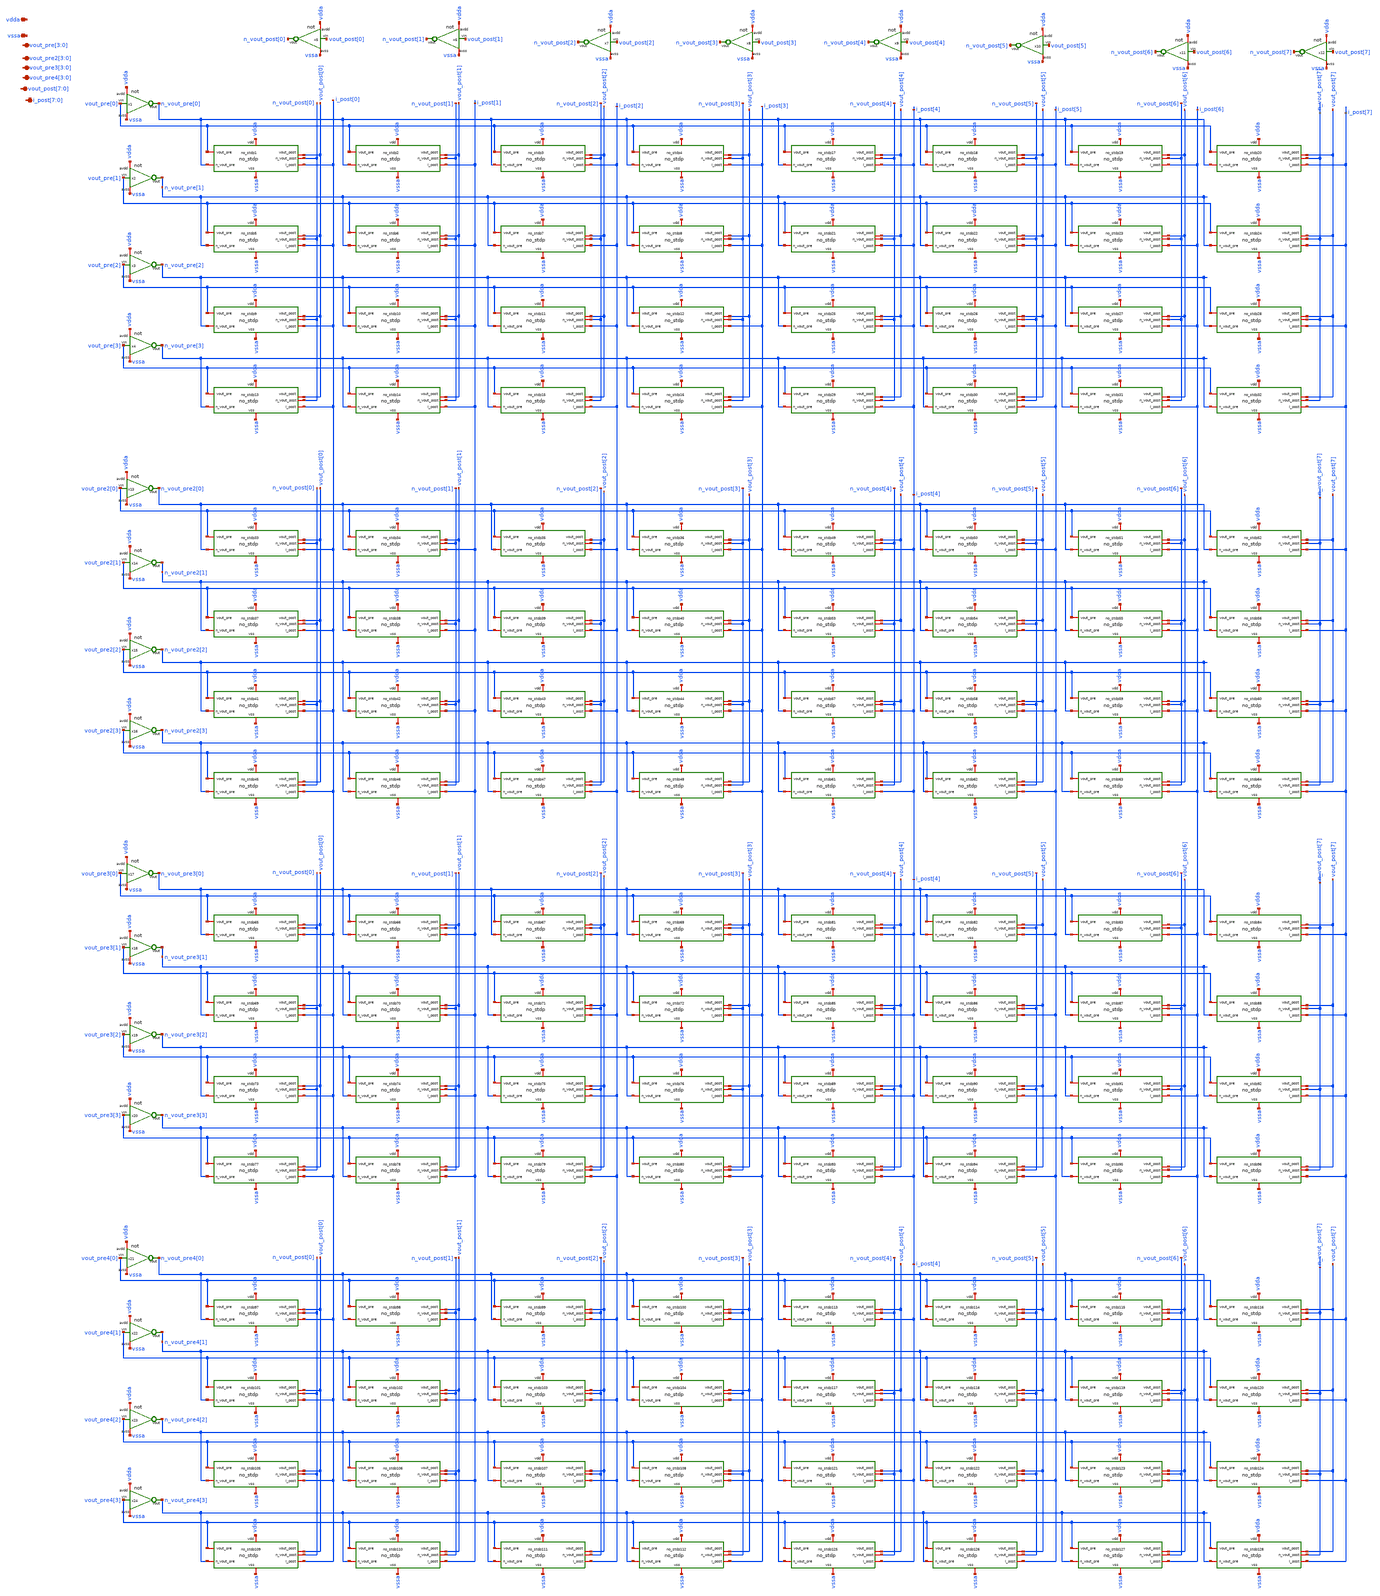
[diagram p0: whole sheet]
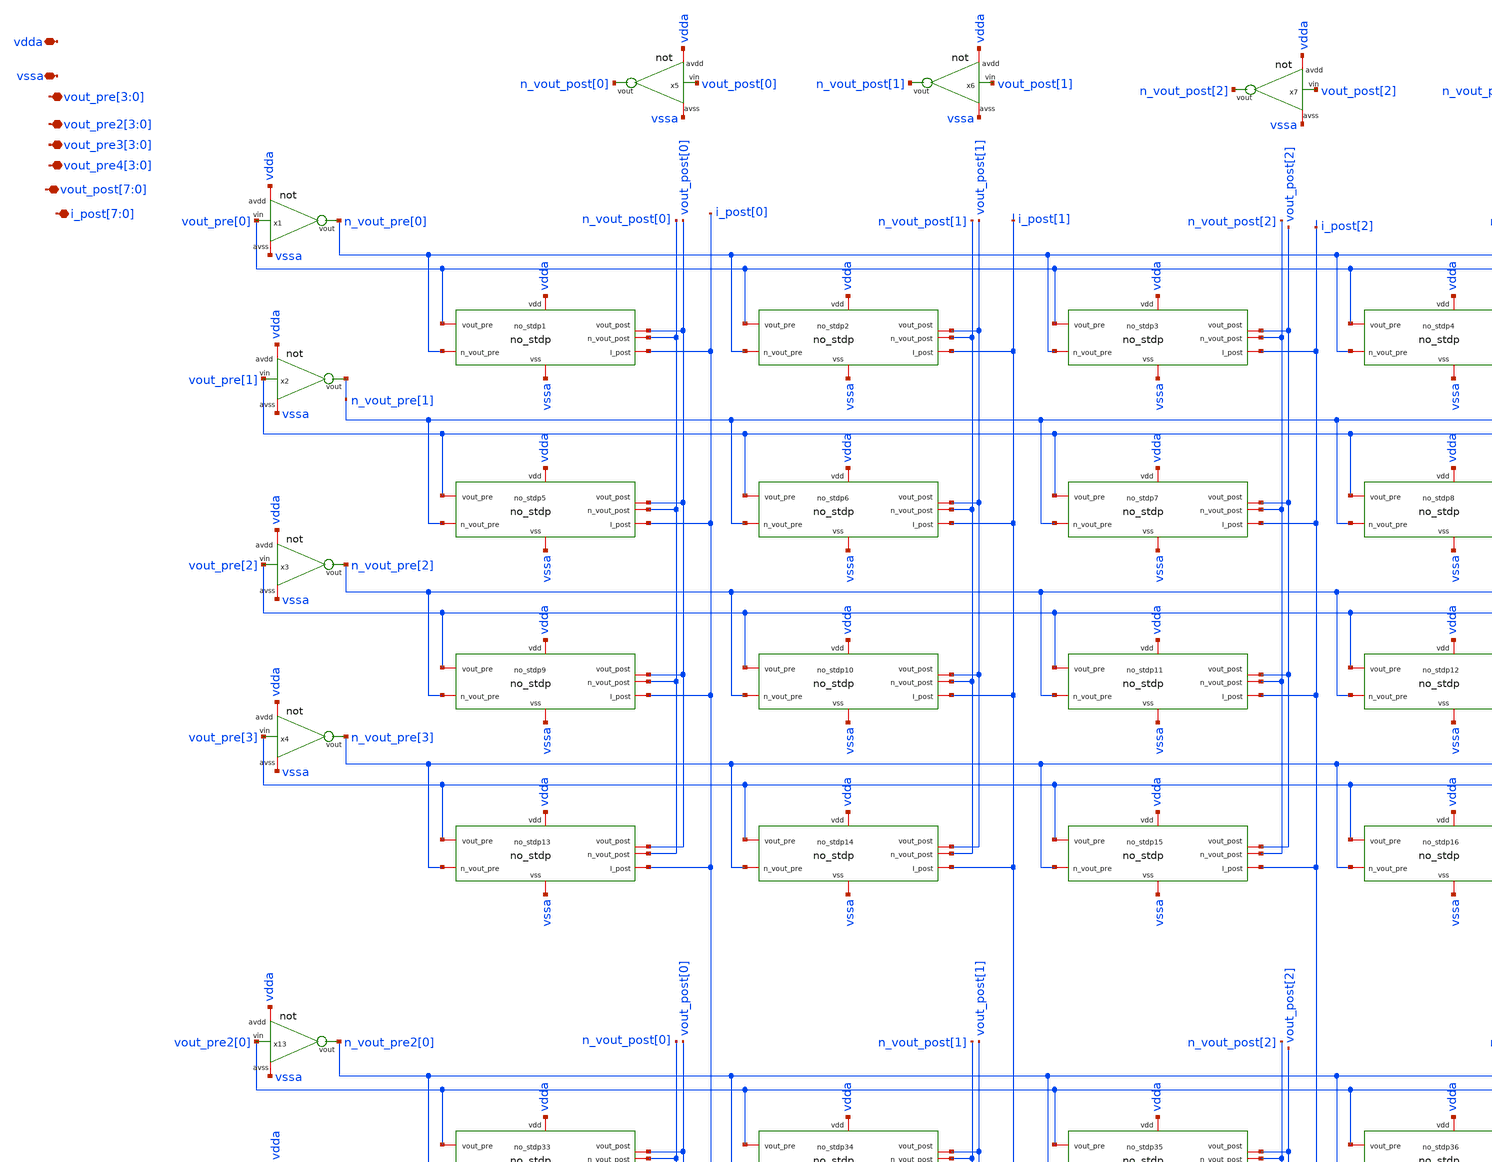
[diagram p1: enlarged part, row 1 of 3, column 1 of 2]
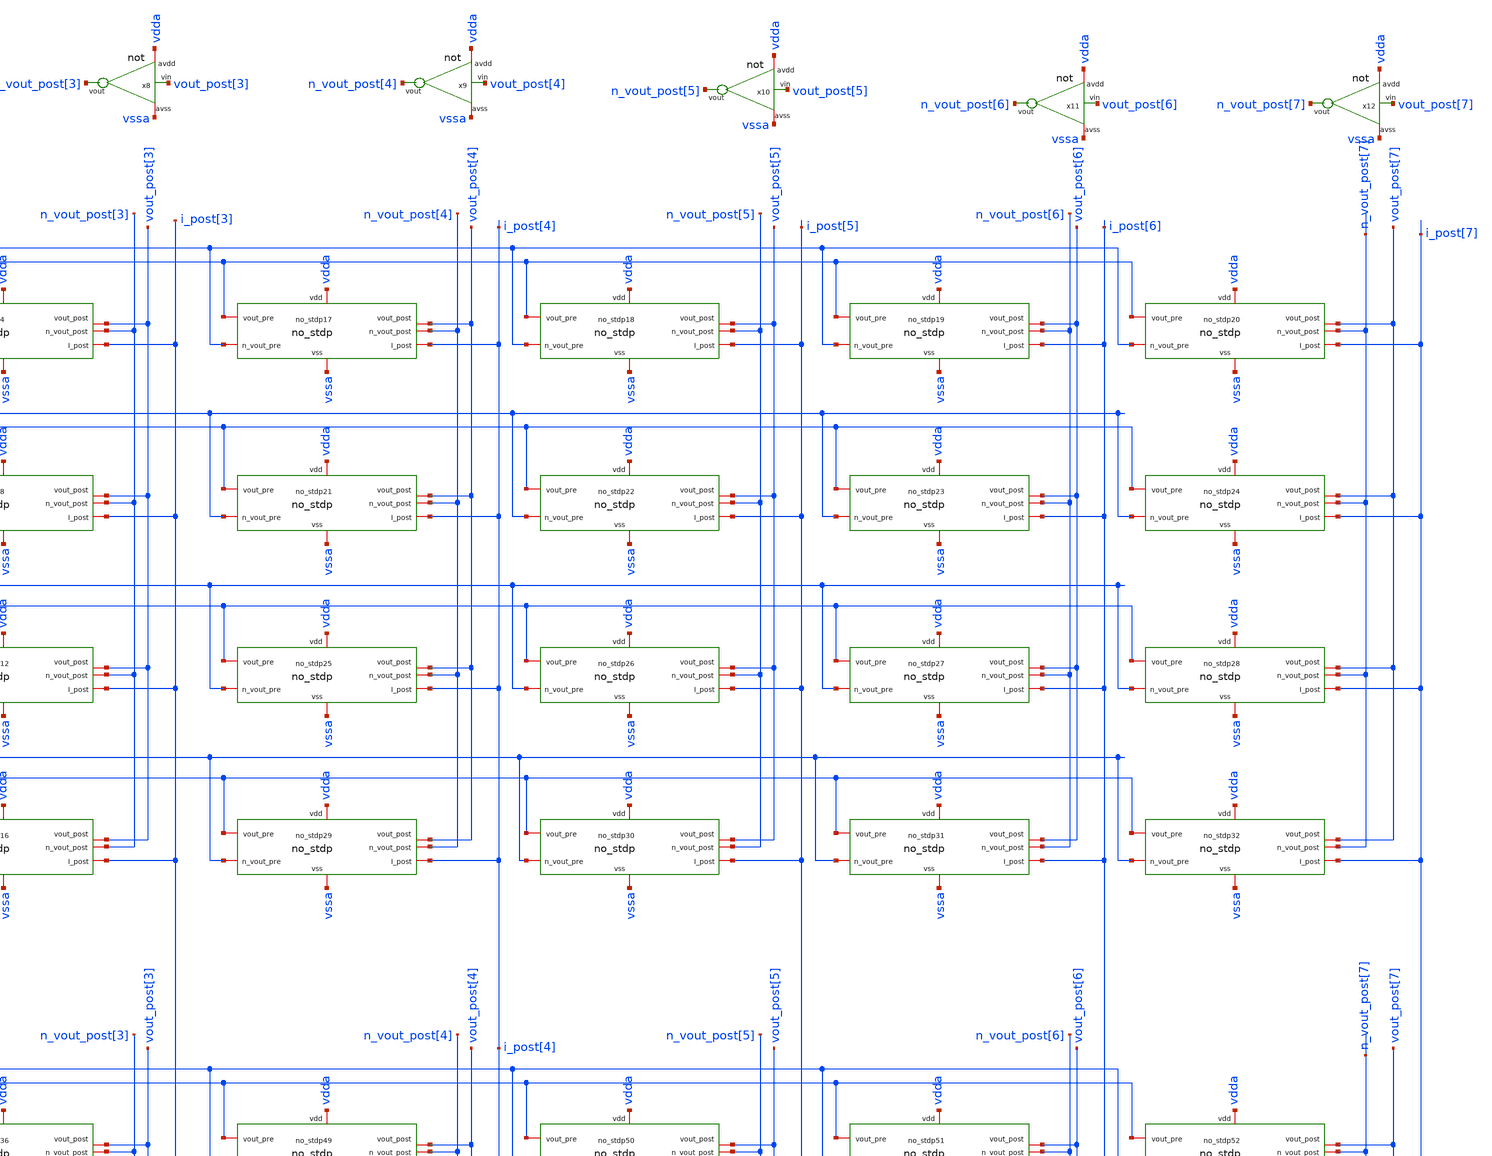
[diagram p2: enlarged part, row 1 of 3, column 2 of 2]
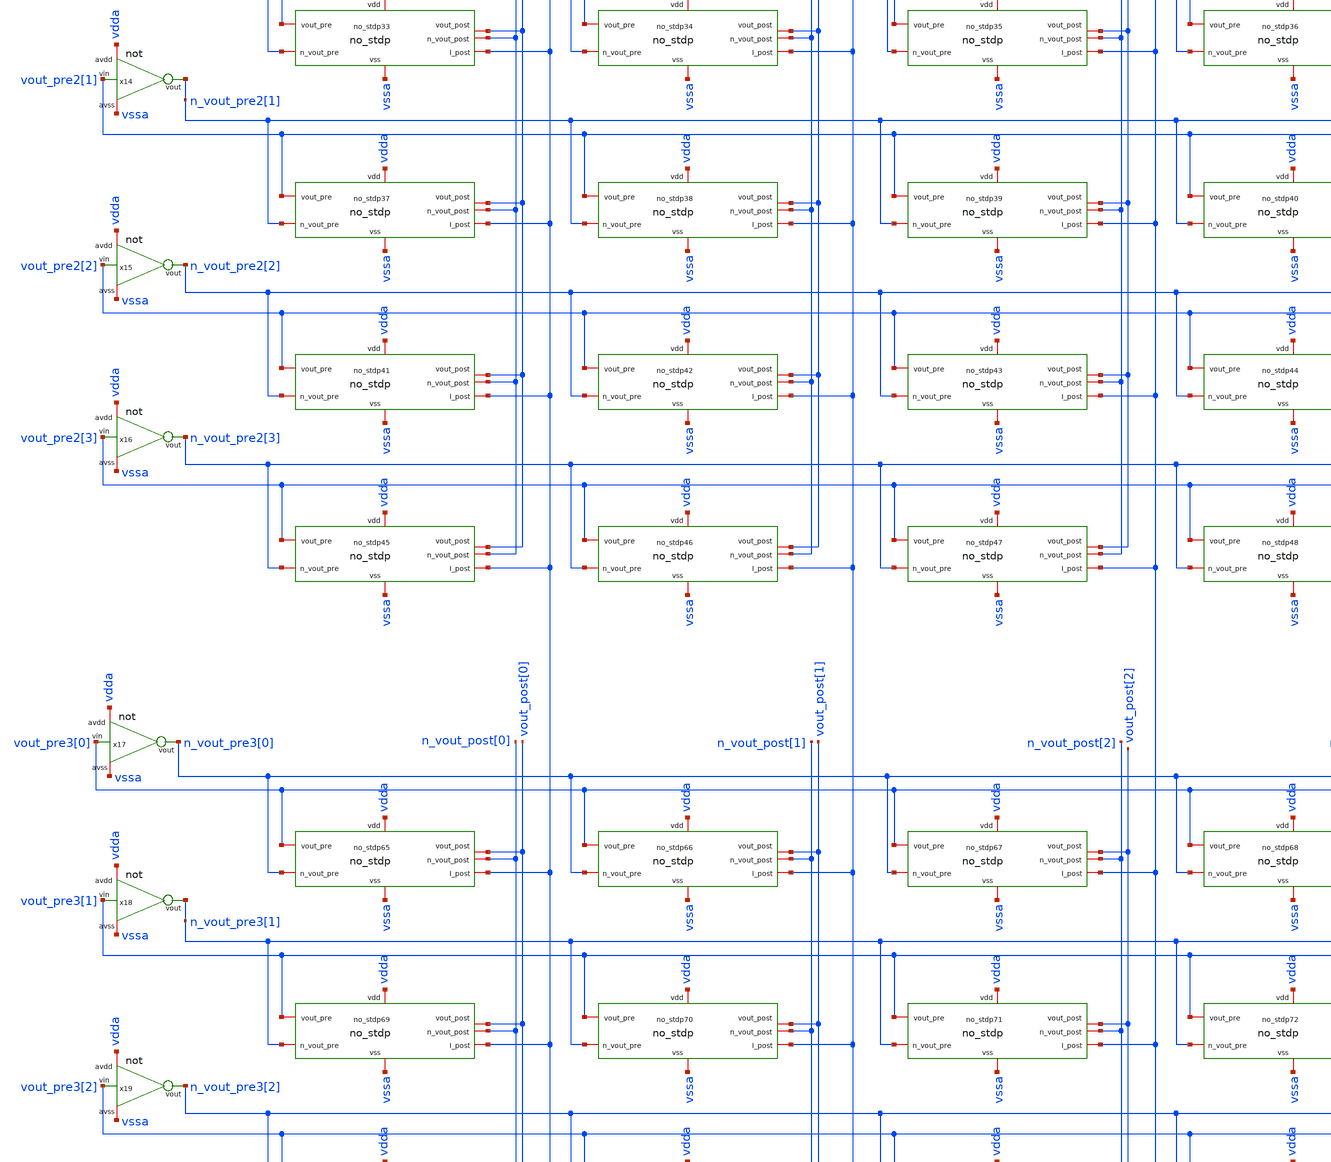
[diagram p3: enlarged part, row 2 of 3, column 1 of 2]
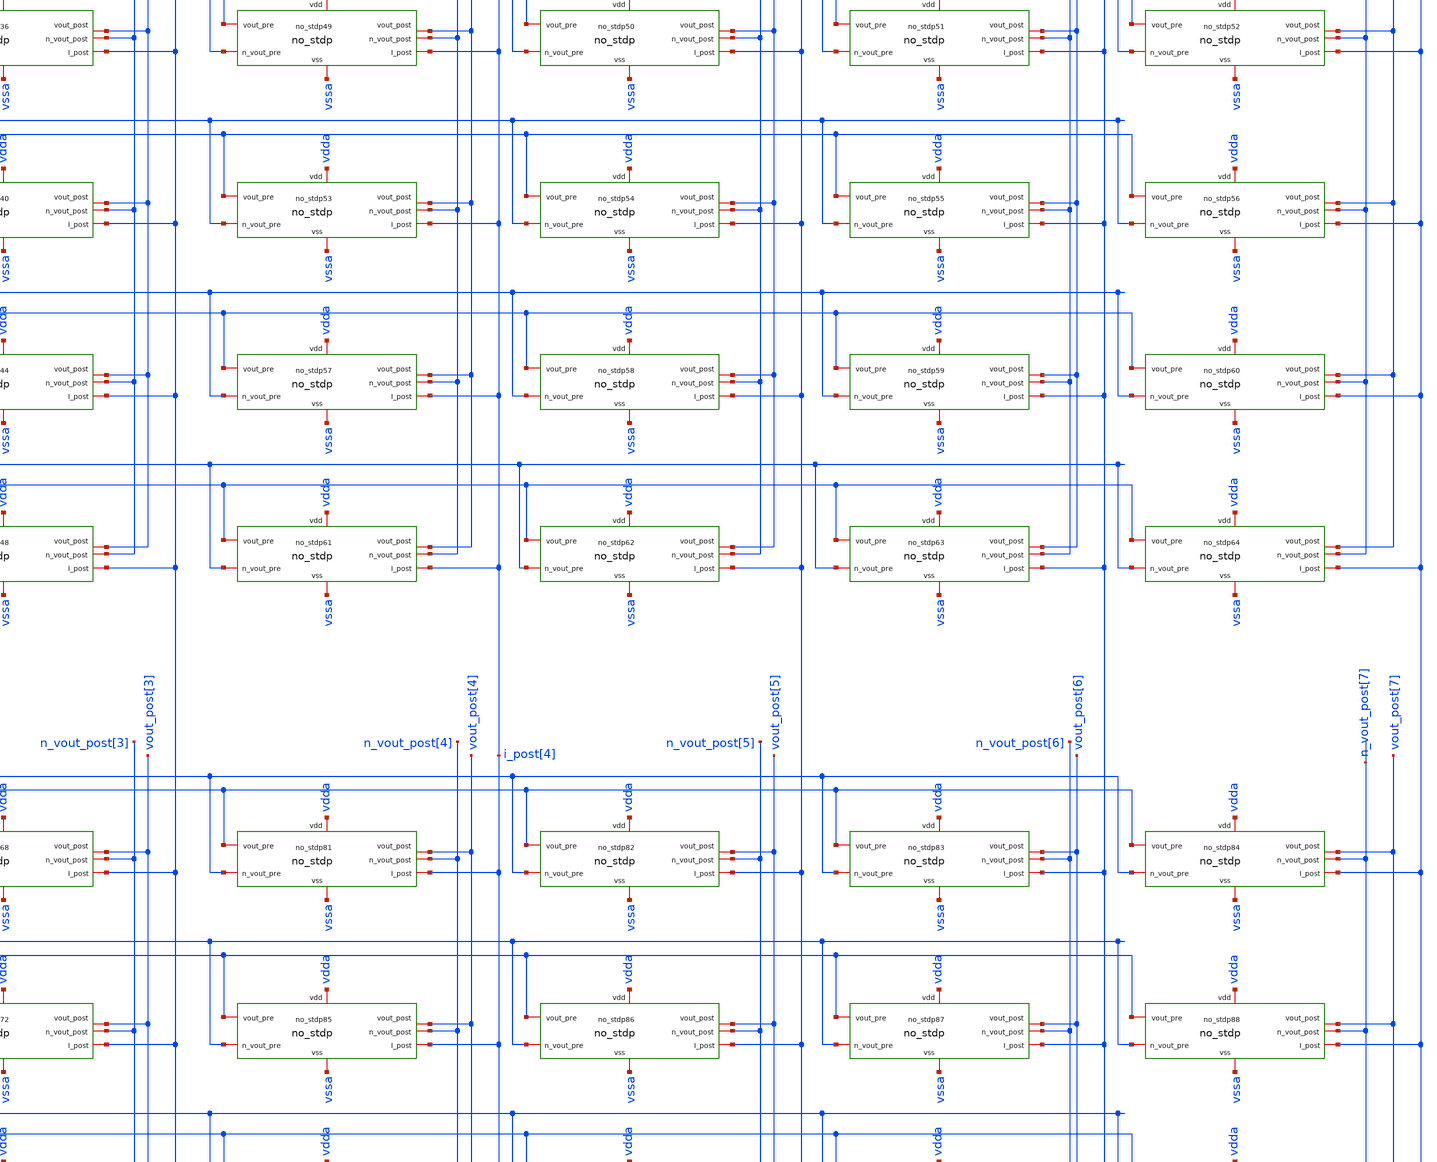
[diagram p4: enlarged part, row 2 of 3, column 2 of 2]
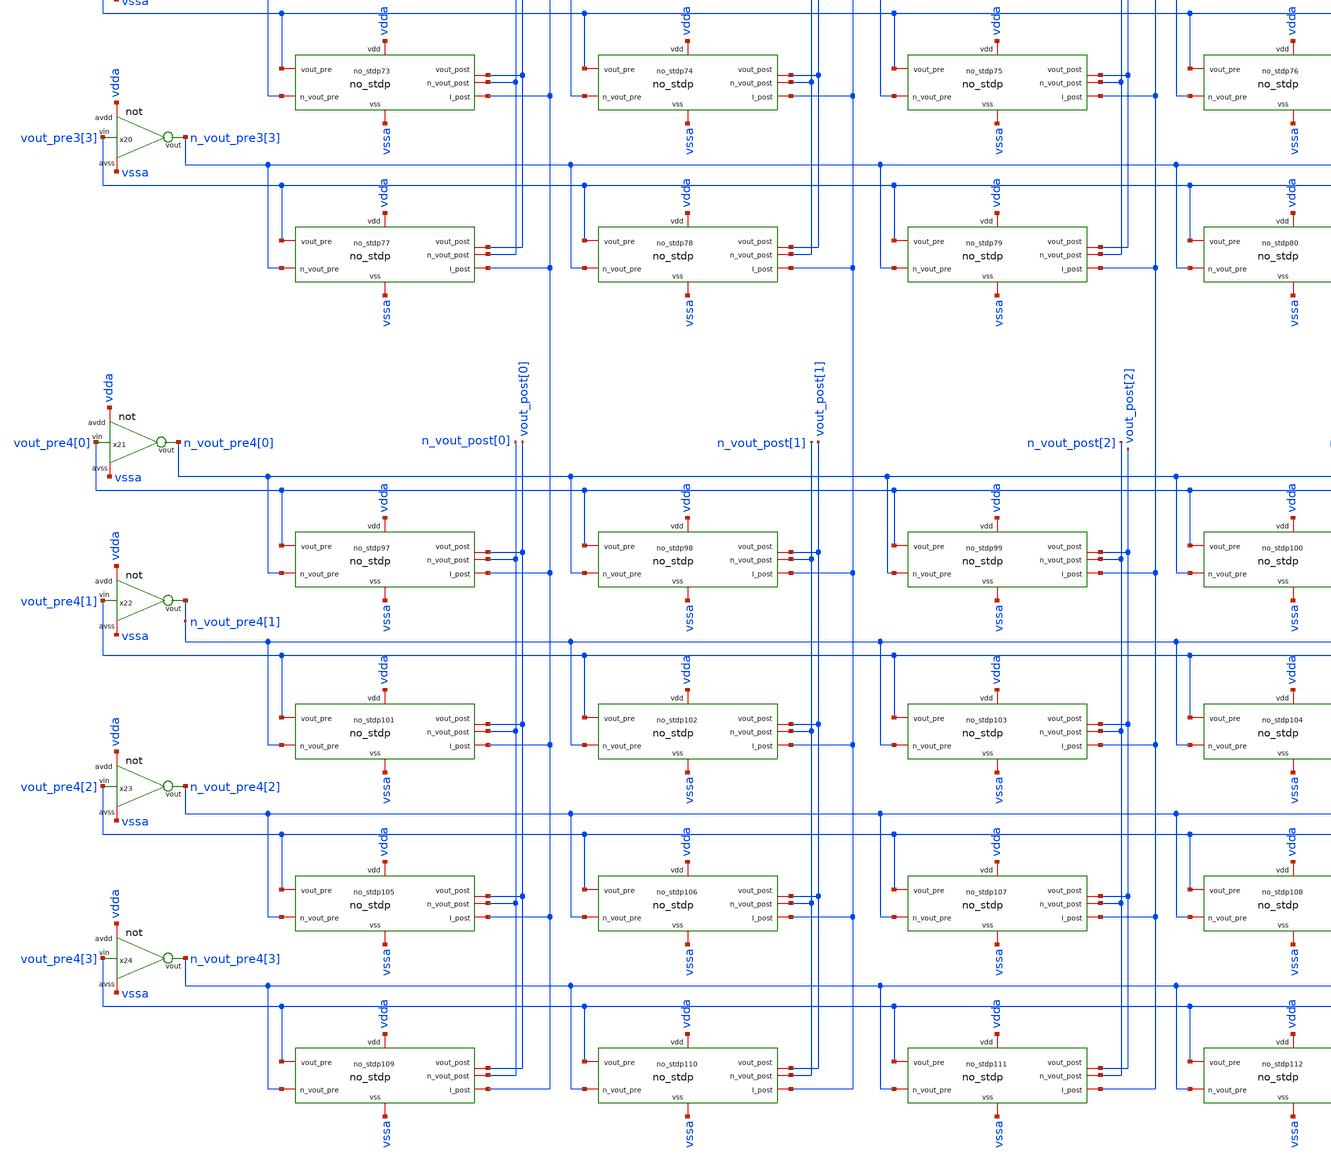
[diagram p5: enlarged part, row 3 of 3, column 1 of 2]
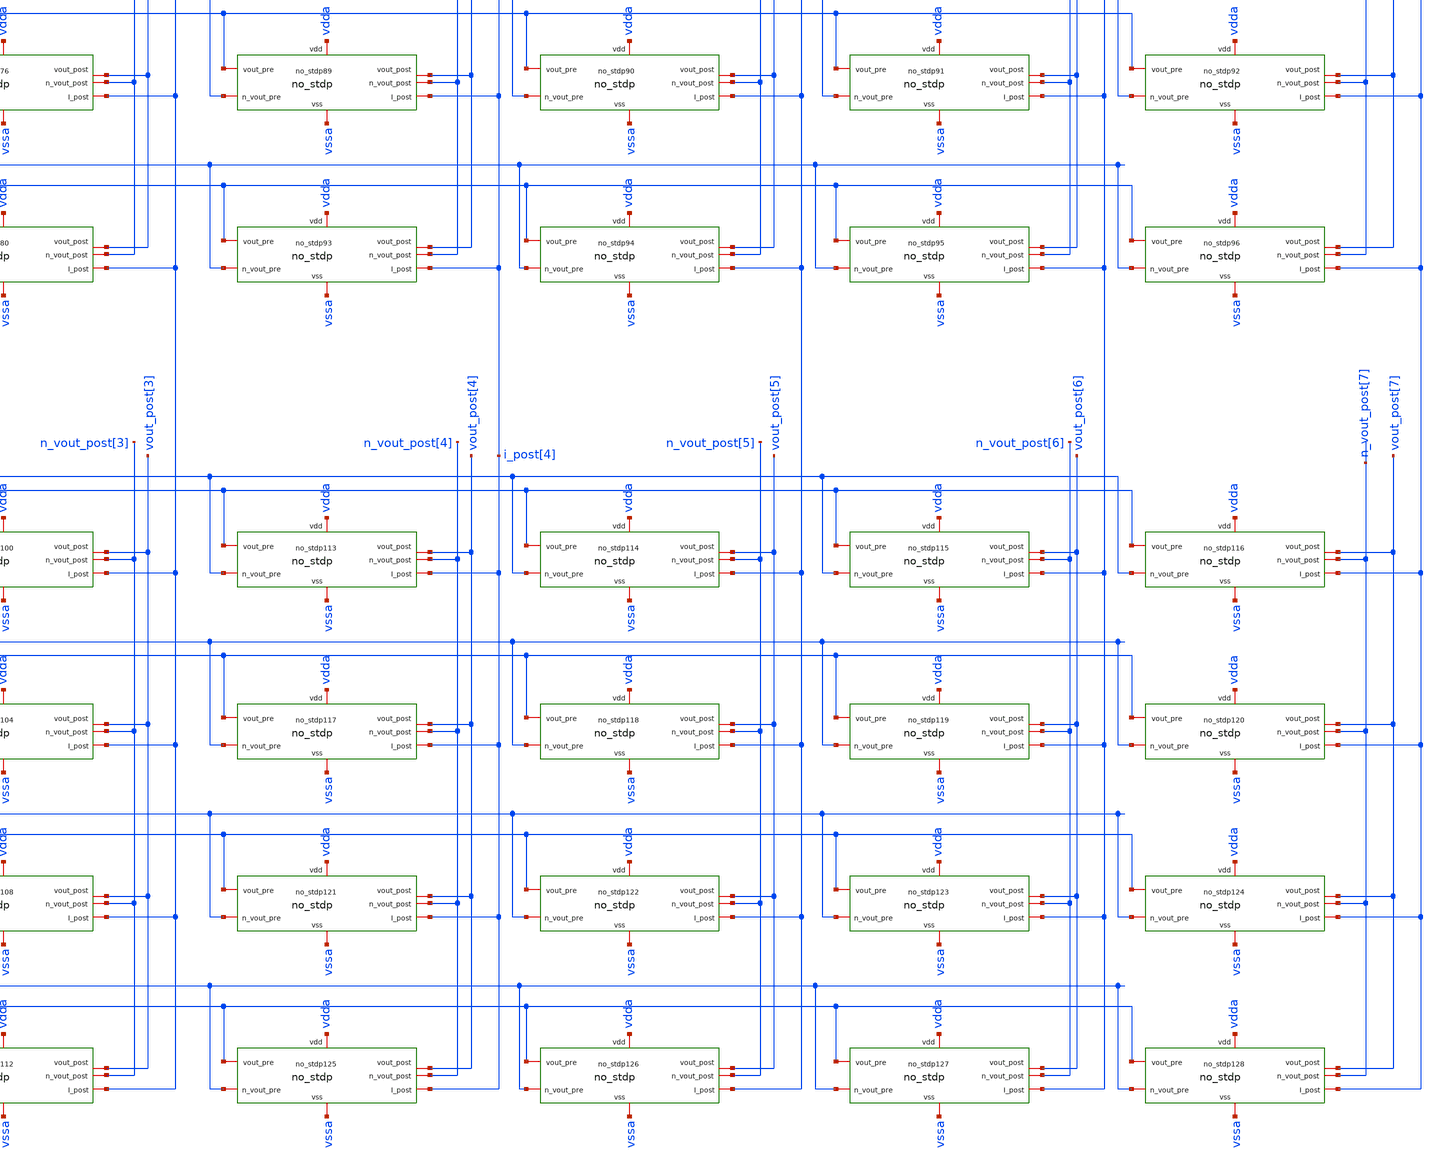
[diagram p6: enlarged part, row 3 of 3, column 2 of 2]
** sch_path: Synapse/no_stdp_4x4x8.sch
**.subckt no_stdp_4x4x8 vdda vssa vout_pre[3],vout_pre[2],vout_pre[1],vout_pre[0]
*+ vout_post[7],vout_post[6],vout_post[5],vout_post[4],vout_post[3],vout_post[2],vout_post[1],vout_post[0] i_post[7],i_post[6],i_post[5],i_post[4],i_post[3],i_post[2],i_post[1],i_post[0]
*+ vout_pre2[3],vout_pre2[2],vout_pre2[1],vout_pre2[0] vout_pre3[3],vout_pre3[2],vout_pre3[1],vout_pre3[0]
*+ vout_pre4[3],vout_pre4[2],vout_pre4[1],vout_pre4[0]
*.iopin vdda
*.iopin vssa
*.iopin vout_pre[3],vout_pre[2],vout_pre[1],vout_pre[0]
*.iopin
*+ vout_post[7],vout_post[6],vout_post[5],vout_post[4],vout_post[3],vout_post[2],vout_post[1],vout_post[0]
*.iopin i_post[7],i_post[6],i_post[5],i_post[4],i_post[3],i_post[2],i_post[1],i_post[0]
*.iopin vout_pre2[3],vout_pre2[2],vout_pre2[1],vout_pre2[0]
*.iopin vout_pre3[3],vout_pre3[2],vout_pre3[1],vout_pre3[0]
*.iopin vout_pre4[3],vout_pre4[2],vout_pre4[1],vout_pre4[0]
xno_stdp1 vdda vssa vout_pre[0] vout_post[0] i_post[0] n_vout_pre[0] n_vout_post[0] no_stdp
xno_stdp2 vdda vssa vout_pre[0] vout_post[1] i_post[1] n_vout_pre[0] n_vout_post[1] no_stdp
xno_stdp3 vdda vssa vout_pre[0] vout_post[2] i_post[2] n_vout_pre[0] n_vout_post[2] no_stdp
xno_stdp4 vdda vssa vout_pre[0] vout_post[3] i_post[3] n_vout_pre[0] n_vout_post[3] no_stdp
xno_stdp5 vdda vssa vout_pre[1] vout_post[0] i_post[0] n_vout_pre[1] n_vout_post[0] no_stdp
xno_stdp6 vdda vssa vout_pre[1] vout_post[1] i_post[1] n_vout_pre[1] n_vout_post[1] no_stdp
xno_stdp7 vdda vssa vout_pre[1] vout_post[2] i_post[2] n_vout_pre[1] n_vout_post[2] no_stdp
xno_stdp8 vdda vssa vout_pre[1] vout_post[3] i_post[3] n_vout_pre[1] n_vout_post[3] no_stdp
xno_stdp9 vdda vssa vout_pre[2] vout_post[0] i_post[0] n_vout_pre[2] n_vout_post[0] no_stdp
xno_stdp10 vdda vssa vout_pre[2] vout_post[1] i_post[1] n_vout_pre[2] n_vout_post[1] no_stdp
xno_stdp11 vdda vssa vout_pre[2] vout_post[2] i_post[2] n_vout_pre[2] n_vout_post[2] no_stdp
xno_stdp12 vdda vssa vout_pre[2] vout_post[3] i_post[3] n_vout_pre[2] n_vout_post[3] no_stdp
xno_stdp13 vdda vssa vout_pre[3] vout_post[0] i_post[0] n_vout_pre[3] n_vout_post[0] no_stdp
xno_stdp14 vdda vssa vout_pre[3] vout_post[1] i_post[1] n_vout_pre[3] n_vout_post[1] no_stdp
xno_stdp15 vdda vssa vout_pre[3] vout_post[2] i_post[2] n_vout_pre[3] n_vout_post[2] no_stdp
xno_stdp16 vdda vssa vout_pre[3] vout_post[3] i_post[3] n_vout_pre[3] n_vout_post[3] no_stdp
xno_stdp17 vdda vssa vout_pre[0] vout_post[4] i_post[4] n_vout_pre[0] n_vout_post[4] no_stdp
xno_stdp18 vdda vssa vout_pre[0] vout_post[5] i_post[5] n_vout_pre[0] n_vout_post[5] no_stdp
xno_stdp19 vdda vssa vout_pre[0] vout_post[6] i_post[6] n_vout_pre[0] n_vout_post[6] no_stdp
xno_stdp20 vdda vssa vout_pre[0] vout_post[7] i_post[7] n_vout_pre[0] n_vout_post[7] no_stdp
xno_stdp21 vdda vssa vout_pre[1] vout_post[4] i_post[4] n_vout_pre[1] n_vout_post[4] no_stdp
xno_stdp22 vdda vssa vout_pre[1] vout_post[5] i_post[5] n_vout_pre[1] n_vout_post[5] no_stdp
xno_stdp23 vdda vssa vout_pre[1] vout_post[6] i_post[6] n_vout_pre[1] n_vout_post[6] no_stdp
xno_stdp24 vdda vssa vout_pre[1] vout_post[7] i_post[7] n_vout_pre[1] n_vout_post[7] no_stdp
xno_stdp25 vdda vssa vout_pre[2] vout_post[4] i_post[4] n_vout_pre[2] n_vout_post[4] no_stdp
xno_stdp26 vdda vssa vout_pre[2] vout_post[5] i_post[5] n_vout_pre[2] n_vout_post[5] no_stdp
xno_stdp27 vdda vssa vout_pre[2] vout_post[6] i_post[6] n_vout_pre[2] n_vout_post[6] no_stdp
xno_stdp28 vdda vssa vout_pre[2] vout_post[7] i_post[7] n_vout_pre[2] n_vout_post[7] no_stdp
xno_stdp29 vdda vssa vout_pre[3] vout_post[4] i_post[4] n_vout_pre[3] n_vout_post[4] no_stdp
xno_stdp30 vdda vssa vout_pre[3] vout_post[5] i_post[5] n_vout_pre[3] n_vout_post[5] no_stdp
xno_stdp31 vdda vssa vout_pre[3] vout_post[6] i_post[6] n_vout_pre[3] n_vout_post[6] no_stdp
xno_stdp32 vdda vssa vout_pre[3] vout_post[7] i_post[7] n_vout_pre[3] n_vout_post[7] no_stdp
x1 vdda vout_pre[0] n_vout_pre[0] vssa not
x2 vdda vout_pre[1] n_vout_pre[1] vssa not
x3 vdda vout_pre[2] n_vout_pre[2] vssa not
x4 vdda vout_pre[3] n_vout_pre[3] vssa not
x5 vdda vout_post[0] n_vout_post[0] vssa not
x6 vdda vout_post[1] n_vout_post[1] vssa not
x7 vdda vout_post[2] n_vout_post[2] vssa not
x8 vdda vout_post[3] n_vout_post[3] vssa not
x9 vdda vout_post[4] n_vout_post[4] vssa not
x10 vdda vout_post[5] n_vout_post[5] vssa not
x11 vdda vout_post[6] n_vout_post[6] vssa not
x12 vdda vout_post[7] n_vout_post[7] vssa not
xno_stdp33 vdda vssa vout_pre2[0] vout_post[0] i_post[0] n_vout_pre2[0] n_vout_post[0] no_stdp
xno_stdp34 vdda vssa vout_pre2[0] vout_post[1] i_post[1] n_vout_pre2[0] n_vout_post[1] no_stdp
xno_stdp35 vdda vssa vout_pre2[0] vout_post[2] i_post[2] n_vout_pre2[0] n_vout_post[2] no_stdp
xno_stdp36 vdda vssa vout_pre2[0] vout_post[3] i_post[3] n_vout_pre2[0] n_vout_post[3] no_stdp
xno_stdp37 vdda vssa vout_pre2[1] vout_post[0] i_post[0] n_vout_pre2[1] n_vout_post[0] no_stdp
xno_stdp38 vdda vssa vout_pre2[1] vout_post[1] i_post[1] n_vout_pre2[1] n_vout_post[1] no_stdp
xno_stdp39 vdda vssa vout_pre2[1] vout_post[2] i_post[2] n_vout_pre2[1] n_vout_post[2] no_stdp
xno_stdp40 vdda vssa vout_pre2[1] vout_post[3] i_post[3] n_vout_pre2[1] n_vout_post[3] no_stdp
xno_stdp41 vdda vssa vout_pre2[2] vout_post[0] i_post[0] n_vout_pre2[2] n_vout_post[0] no_stdp
xno_stdp42 vdda vssa vout_pre2[2] vout_post[1] i_post[1] n_vout_pre2[2] n_vout_post[1] no_stdp
xno_stdp43 vdda vssa vout_pre2[2] vout_post[2] i_post[2] n_vout_pre2[2] n_vout_post[2] no_stdp
xno_stdp44 vdda vssa vout_pre2[2] vout_post[3] i_post[3] n_vout_pre2[2] n_vout_post[3] no_stdp
xno_stdp45 vdda vssa vout_pre2[3] vout_post[0] i_post[0] n_vout_pre2[3] n_vout_post[0] no_stdp
xno_stdp46 vdda vssa vout_pre2[3] vout_post[1] i_post[1] n_vout_pre2[3] n_vout_post[1] no_stdp
xno_stdp47 vdda vssa vout_pre2[3] vout_post[2] i_post[2] n_vout_pre2[3] n_vout_post[2] no_stdp
xno_stdp48 vdda vssa vout_pre2[3] vout_post[3] i_post[3] n_vout_pre2[3] n_vout_post[3] no_stdp
xno_stdp49 vdda vssa vout_pre2[0] vout_post[4] i_post[4] n_vout_pre2[0] n_vout_post[4] no_stdp
xno_stdp50 vdda vssa vout_pre2[0] vout_post[5] i_post[5] n_vout_pre2[0] n_vout_post[5] no_stdp
xno_stdp51 vdda vssa vout_pre2[0] vout_post[6] i_post[6] n_vout_pre2[0] n_vout_post[6] no_stdp
xno_stdp52 vdda vssa vout_pre2[0] vout_post[7] i_post[7] n_vout_pre2[0] n_vout_post[7] no_stdp
xno_stdp53 vdda vssa vout_pre2[1] vout_post[4] i_post[4] n_vout_pre2[1] n_vout_post[4] no_stdp
xno_stdp54 vdda vssa vout_pre2[1] vout_post[5] i_post[5] n_vout_pre2[1] n_vout_post[5] no_stdp
xno_stdp55 vdda vssa vout_pre2[1] vout_post[6] i_post[6] n_vout_pre2[1] n_vout_post[6] no_stdp
xno_stdp56 vdda vssa vout_pre2[1] vout_post[7] i_post[7] n_vout_pre2[1] n_vout_post[7] no_stdp
xno_stdp57 vdda vssa vout_pre2[2] vout_post[4] i_post[4] n_vout_pre2[2] n_vout_post[4] no_stdp
xno_stdp58 vdda vssa vout_pre2[2] vout_post[5] i_post[5] n_vout_pre2[2] n_vout_post[5] no_stdp
xno_stdp59 vdda vssa vout_pre2[2] vout_post[6] i_post[6] n_vout_pre2[2] n_vout_post[6] no_stdp
xno_stdp60 vdda vssa vout_pre2[2] vout_post[7] i_post[7] n_vout_pre2[2] n_vout_post[7] no_stdp
xno_stdp61 vdda vssa vout_pre2[3] vout_post[4] i_post[4] n_vout_pre2[3] n_vout_post[4] no_stdp
xno_stdp62 vdda vssa vout_pre2[3] vout_post[5] i_post[5] n_vout_pre2[3] n_vout_post[5] no_stdp
xno_stdp63 vdda vssa vout_pre2[3] vout_post[6] i_post[6] n_vout_pre2[3] n_vout_post[6] no_stdp
xno_stdp64 vdda vssa vout_pre2[3] vout_post[7] i_post[7] n_vout_pre2[3] n_vout_post[7] no_stdp
x13 vdda vout_pre2[0] n_vout_pre2[0] vssa not
x14 vdda vout_pre2[1] n_vout_pre2[1] vssa not
x15 vdda vout_pre2[2] n_vout_pre2[2] vssa not
x16 vdda vout_pre2[3] n_vout_pre2[3] vssa not
xno_stdp65 vdda vssa vout_pre3[0] vout_post[0] i_post[0] n_vout_pre3[0] n_vout_post[0] no_stdp
xno_stdp66 vdda vssa vout_pre3[0] vout_post[1] i_post[1] n_vout_pre3[0] n_vout_post[1] no_stdp
xno_stdp67 vdda vssa vout_pre3[0] vout_post[2] i_post[2] n_vout_pre3[0] n_vout_post[2] no_stdp
xno_stdp68 vdda vssa vout_pre3[0] vout_post[3] i_post[3] n_vout_pre3[0] n_vout_post[3] no_stdp
xno_stdp69 vdda vssa vout_pre3[1] vout_post[0] i_post[0] n_vout_pre3[1] n_vout_post[0] no_stdp
xno_stdp70 vdda vssa vout_pre3[1] vout_post[1] i_post[1] n_vout_pre3[1] n_vout_post[1] no_stdp
xno_stdp71 vdda vssa vout_pre3[1] vout_post[2] i_post[2] n_vout_pre3[1] n_vout_post[2] no_stdp
xno_stdp72 vdda vssa vout_pre3[1] vout_post[3] i_post[3] n_vout_pre3[1] n_vout_post[3] no_stdp
xno_stdp73 vdda vssa vout_pre3[2] vout_post[0] i_post[0] n_vout_pre3[2] n_vout_post[0] no_stdp
xno_stdp74 vdda vssa vout_pre3[2] vout_post[1] i_post[1] n_vout_pre3[2] n_vout_post[1] no_stdp
xno_stdp75 vdda vssa vout_pre3[2] vout_post[2] i_post[2] n_vout_pre3[2] n_vout_post[2] no_stdp
xno_stdp76 vdda vssa vout_pre3[2] vout_post[3] i_post[3] n_vout_pre3[2] n_vout_post[3] no_stdp
xno_stdp77 vdda vssa vout_pre3[3] vout_post[0] i_post[0] n_vout_pre3[3] n_vout_post[0] no_stdp
xno_stdp78 vdda vssa vout_pre3[3] vout_post[1] i_post[1] n_vout_pre3[3] n_vout_post[1] no_stdp
xno_stdp79 vdda vssa vout_pre3[3] vout_post[2] i_post[2] n_vout_pre3[3] n_vout_post[2] no_stdp
xno_stdp80 vdda vssa vout_pre3[3] vout_post[3] i_post[3] n_vout_pre3[3] n_vout_post[3] no_stdp
xno_stdp81 vdda vssa vout_pre3[0] vout_post[4] i_post[4] n_vout_pre3[0] n_vout_post[4] no_stdp
xno_stdp82 vdda vssa vout_pre3[0] vout_post[5] i_post[5] n_vout_pre3[0] n_vout_post[5] no_stdp
xno_stdp83 vdda vssa vout_pre3[0] vout_post[6] i_post[6] n_vout_pre3[0] n_vout_post[6] no_stdp
xno_stdp84 vdda vssa vout_pre3[0] vout_post[7] i_post[7] n_vout_pre3[0] n_vout_post[7] no_stdp
xno_stdp85 vdda vssa vout_pre3[1] vout_post[4] i_post[4] n_vout_pre3[1] n_vout_post[4] no_stdp
xno_stdp86 vdda vssa vout_pre3[1] vout_post[5] i_post[5] n_vout_pre3[1] n_vout_post[5] no_stdp
xno_stdp87 vdda vssa vout_pre3[1] vout_post[6] i_post[6] n_vout_pre3[1] n_vout_post[6] no_stdp
xno_stdp88 vdda vssa vout_pre3[1] vout_post[7] i_post[7] n_vout_pre3[1] n_vout_post[7] no_stdp
xno_stdp89 vdda vssa vout_pre3[2] vout_post[4] i_post[4] n_vout_pre3[2] n_vout_post[4] no_stdp
xno_stdp90 vdda vssa vout_pre3[2] vout_post[5] i_post[5] n_vout_pre3[2] n_vout_post[5] no_stdp
xno_stdp91 vdda vssa vout_pre3[2] vout_post[6] i_post[6] n_vout_pre3[2] n_vout_post[6] no_stdp
xno_stdp92 vdda vssa vout_pre3[2] vout_post[7] i_post[7] n_vout_pre3[2] n_vout_post[7] no_stdp
xno_stdp93 vdda vssa vout_pre3[3] vout_post[4] i_post[4] n_vout_pre3[3] n_vout_post[4] no_stdp
xno_stdp94 vdda vssa vout_pre3[3] vout_post[5] i_post[5] n_vout_pre3[3] n_vout_post[5] no_stdp
xno_stdp95 vdda vssa vout_pre3[3] vout_post[6] i_post[6] n_vout_pre3[3] n_vout_post[6] no_stdp
xno_stdp96 vdda vssa vout_pre3[3] vout_post[7] i_post[7] n_vout_pre3[3] n_vout_post[7] no_stdp
x17 vdda vout_pre3[0] n_vout_pre3[0] vssa not
x18 vdda vout_pre3[1] n_vout_pre3[1] vssa not
x19 vdda vout_pre3[2] n_vout_pre3[2] vssa not
x20 vdda vout_pre3[3] n_vout_pre3[3] vssa not
xno_stdp97 vdda vssa vout_pre4[0] vout_post[0] i_post[0] n_vout_pre4[0] n_vout_post[0] no_stdp
xno_stdp98 vdda vssa vout_pre4[0] vout_post[1] i_post[1] n_vout_pre4[0] n_vout_post[1] no_stdp
xno_stdp99 vdda vssa vout_pre4[0] vout_post[2] i_post[2] n_vout_pre4[0] n_vout_post[2] no_stdp
xno_stdp100 vdda vssa vout_pre4[0] vout_post[3] i_post[3] n_vout_pre4[0] n_vout_post[3] no_stdp
xno_stdp101 vdda vssa vout_pre4[1] vout_post[0] i_post[0] n_vout_pre4[1] n_vout_post[0] no_stdp
xno_stdp102 vdda vssa vout_pre4[1] vout_post[1] i_post[1] n_vout_pre4[1] n_vout_post[1] no_stdp
xno_stdp103 vdda vssa vout_pre4[1] vout_post[2] i_post[2] n_vout_pre4[1] n_vout_post[2] no_stdp
xno_stdp104 vdda vssa vout_pre4[1] vout_post[3] i_post[3] n_vout_pre4[1] n_vout_post[3] no_stdp
xno_stdp105 vdda vssa vout_pre4[2] vout_post[0] i_post[0] n_vout_pre4[2] n_vout_post[0] no_stdp
xno_stdp106 vdda vssa vout_pre4[2] vout_post[1] i_post[1] n_vout_pre4[2] n_vout_post[1] no_stdp
xno_stdp107 vdda vssa vout_pre4[2] vout_post[2] i_post[2] n_vout_pre4[2] n_vout_post[2] no_stdp
xno_stdp108 vdda vssa vout_pre4[2] vout_post[3] i_post[3] n_vout_pre4[2] n_vout_post[3] no_stdp
xno_stdp109 vdda vssa vout_pre4[3] vout_post[0] i_post[0] n_vout_pre4[3] n_vout_post[0] no_stdp
xno_stdp110 vdda vssa vout_pre4[3] vout_post[1] i_post[1] n_vout_pre4[3] n_vout_post[1] no_stdp
xno_stdp111 vdda vssa vout_pre4[3] vout_post[2] i_post[2] n_vout_pre4[3] n_vout_post[2] no_stdp
xno_stdp112 vdda vssa vout_pre4[3] vout_post[3] i_post[3] n_vout_pre4[3] n_vout_post[3] no_stdp
xno_stdp113 vdda vssa vout_pre4[0] vout_post[4] i_post[4] n_vout_pre4[0] n_vout_post[4] no_stdp
xno_stdp114 vdda vssa vout_pre4[0] vout_post[5] i_post[5] n_vout_pre4[0] n_vout_post[5] no_stdp
xno_stdp115 vdda vssa vout_pre4[0] vout_post[6] i_post[6] n_vout_pre4[0] n_vout_post[6] no_stdp
xno_stdp116 vdda vssa vout_pre4[0] vout_post[7] i_post[7] n_vout_pre4[0] n_vout_post[7] no_stdp
xno_stdp117 vdda vssa vout_pre4[1] vout_post[4] i_post[4] n_vout_pre4[1] n_vout_post[4] no_stdp
xno_stdp118 vdda vssa vout_pre4[1] vout_post[5] i_post[5] n_vout_pre4[1] n_vout_post[5] no_stdp
xno_stdp119 vdda vssa vout_pre4[1] vout_post[6] i_post[6] n_vout_pre4[1] n_vout_post[6] no_stdp
xno_stdp120 vdda vssa vout_pre4[1] vout_post[7] i_post[7] n_vout_pre4[1] n_vout_post[7] no_stdp
xno_stdp121 vdda vssa vout_pre4[2] vout_post[4] i_post[4] n_vout_pre4[2] n_vout_post[4] no_stdp
xno_stdp122 vdda vssa vout_pre4[2] vout_post[5] i_post[5] n_vout_pre4[2] n_vout_post[5] no_stdp
xno_stdp123 vdda vssa vout_pre4[2] vout_post[6] i_post[6] n_vout_pre4[2] n_vout_post[6] no_stdp
xno_stdp124 vdda vssa vout_pre4[2] vout_post[7] i_post[7] n_vout_pre4[2] n_vout_post[7] no_stdp
xno_stdp125 vdda vssa vout_pre4[3] vout_post[4] i_post[4] n_vout_pre4[3] n_vout_post[4] no_stdp
xno_stdp126 vdda vssa vout_pre4[3] vout_post[5] i_post[5] n_vout_pre4[3] n_vout_post[5] no_stdp
xno_stdp127 vdda vssa vout_pre4[3] vout_post[6] i_post[6] n_vout_pre4[3] n_vout_post[6] no_stdp
xno_stdp128 vdda vssa vout_pre4[3] vout_post[7] i_post[7] n_vout_pre4[3] n_vout_post[7] no_stdp
x21 vdda vout_pre4[0] n_vout_pre4[0] vssa not
x22 vdda vout_pre4[1] n_vout_pre4[1] vssa not
x23 vdda vout_pre4[2] n_vout_pre4[2] vssa not
x24 vdda vout_pre4[3] n_vout_pre4[3] vssa not
**.ends
.end
